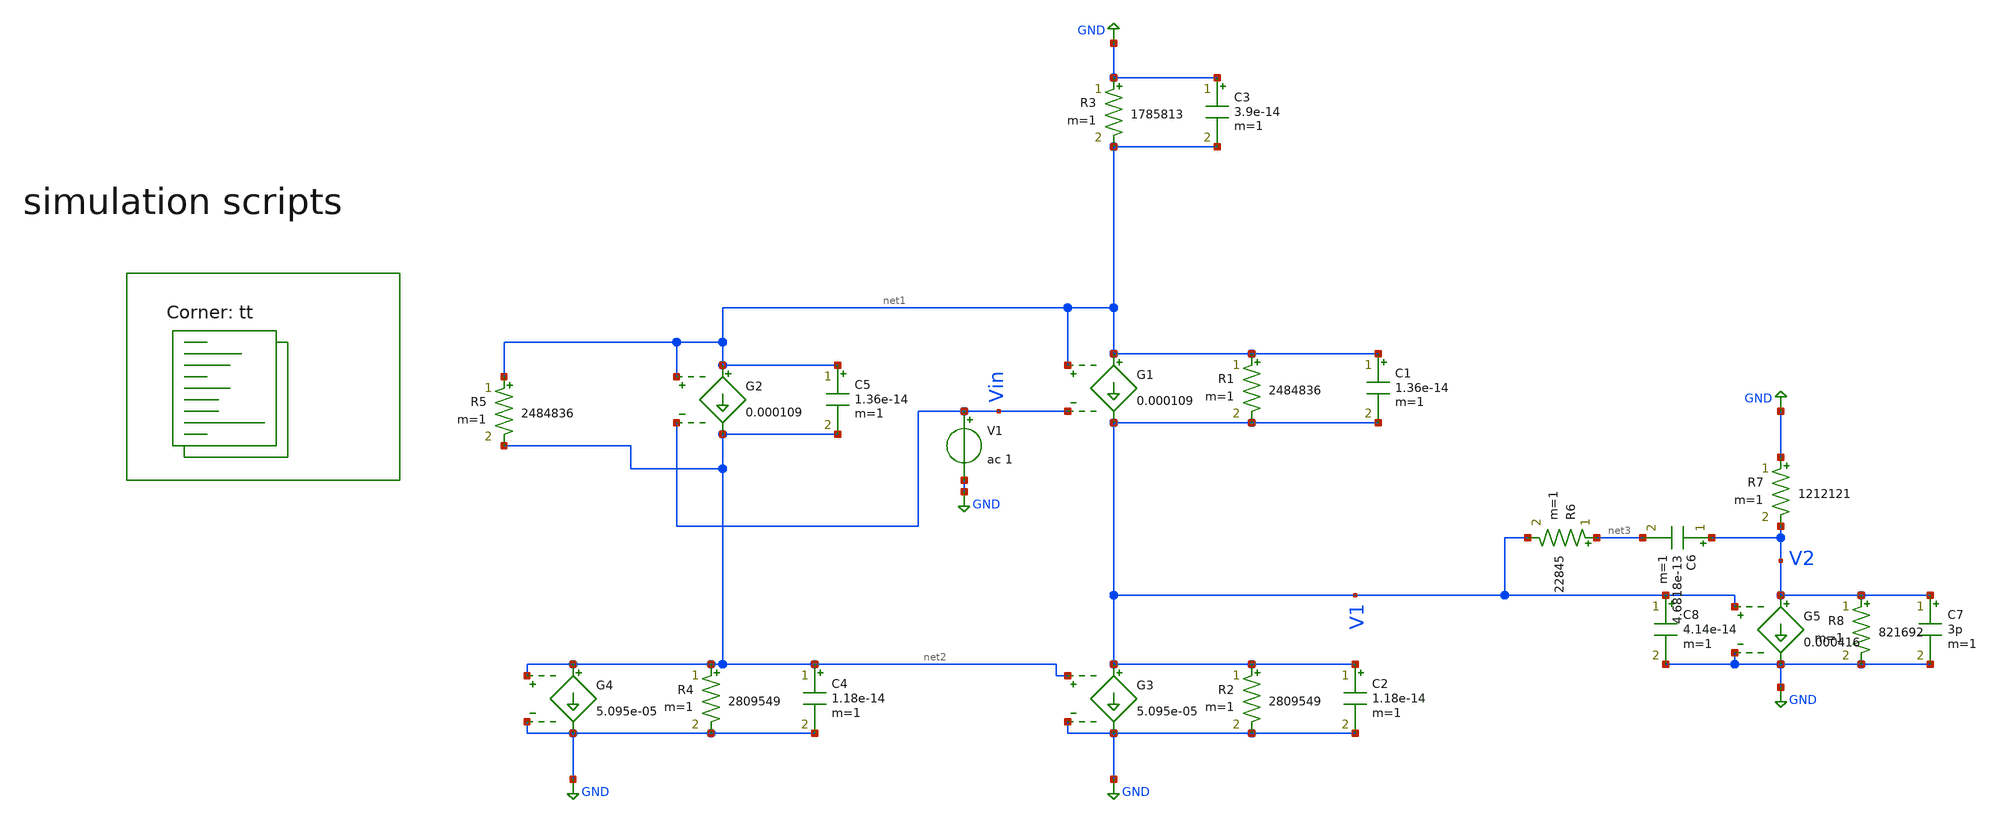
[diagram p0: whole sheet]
** sch_path: Learning/single_ended_amplifiers/Miller_OTA_2_stage_model/full_equivalent_model_ac__common_gain.sch
**.subckt full_equivalent_model_ac__common_gain
V1 Vin GND ac 1
G1 net1 V1 net1 Vin 0.000109
R1 net1 V1 2484836 m=1
R2 V1 GND 2809549 m=1
G3 V1 GND net2 GND 5.095e-05
C2 V1 GND 1.18e-14 m=1
C1 net1 V1 1.36e-14 m=1
R3 GND net1 1785813 m=1
C3 GND net1 3.9e-14 m=1
G2 net1 net2 net1 Vin 0.000109
R4 net2 GND 2809549 m=1
G4 net2 GND net2 GND 5.095e-05
R5 net1 net2 2484836 m=1
C5 net1 net2 1.36e-14 m=1
G5 V2 GND V1 GND 0.000416
R6 net3 V1 22845 m=1
C6 V2 net3 4.6818e-13 m=1
R7 GND V2 1212121 m=1
C7 V2 GND 3p m=1
R8 V2 GND 821692 m=1
C8 V1 GND 4.14e-14 m=1
C4 net2 GND 1.18e-14 m=1
**** begin user architecture code
.lib $::SKYWATER_MODELS/sky130.lib.spice tt

.Temp 27
.param VDD = 5
.param VSS = 0



.control
save all
ac dec 100 1 10G
plot db(v(V2)) (180+(180*ph(v(V2))/pi)) db(v(V1))
pz VIN 0 0 V2 vol pz
print all




.endc


**** end user architecture code
**.ends
.GLOBAL GND
.end
